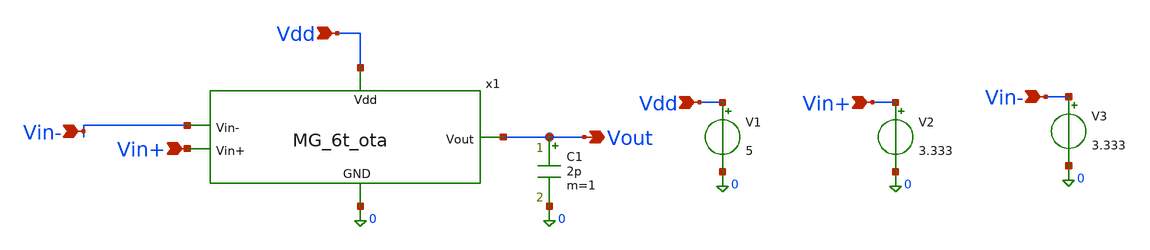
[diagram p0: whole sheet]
** sch_path: MG_6T_OTA/MG_6t_ota_testbench.sch
**.subckt MG_6t_ota_testbench Vdd Vin+ Vin- Vdd Vin+ Vin- Vout
*.ipin Vdd
*.ipin Vin+
*.ipin Vin-
*.ipin Vdd
*.ipin Vin+
*.ipin Vin-
*.opin Vout
V1 Vdd 0 5
V2 Vin+ 0 3.333
V3 Vin- 0 3.333
C1 Vout 0 2p m=1
x1 Vdd Vout Vin- Vin+ 0 MG_6t_ota
**** begin user architecture code



*.include /foss/pdks/gf180mcuD/libs.tech/ngspice/design.ngspice
*.lib /foss/pdks/gf180mcuD/libs.tech/ngspice/sm141064.ngspice typical
*.lib /foss/pdks/gf180mcuD/libs.tech/ngspice/sm141064.ngspice res_typical
*.lib /foss/pdks/gf180mcuD/libs.tech/ngspice/sm141064.ngspice moscap_typical
*.lib /foss/pdks/gf180mcuD/libs.tech/ngspice/sm141064.ngspice diode_typical

*.control
*  save all
*  op
*  alter v2 ac = 1
*  ac dec 20 1 1G
*  setplot ac1
*
*  let gain_db = vdb(vout)
*  let phase_deg = (180/PI) * ph(vout)
*
*  meas ac dc_gain MAX gain_db
*  meas ac ugbw WHEN gain_db=0 FALL=1
*  meas ac ph_at_ugbw FIND phase_deg WHEN gain_db=0
*  let phase_margin = 180 + ph_at_ugbw
*
*  print dc_gain ugbw phase_margin
*
*  plot gain_db title 'Magnitude Response (dB)'
*  plot phase_deg title 'Phase Response (Degrees)'
*.endc

.include /foss/pdks/gf180mcuD/libs.tech/ngspice/design.ngspice

* MUST be defined here exactly as 1
.param sw_stat_global=1
.param sw_stat_mismatch=1

.lib /foss/pdks/gf180mcuD/libs.tech/ngspice/sm141064.ngspice statistical
.lib /foss/pdks/gf180mcuD/libs.tech/ngspice/sm141064.ngspice res_statistical
.lib /foss/pdks/gf180mcuD/libs.tech/ngspice/sm141064.ngspice moscap_typical
.lib /foss/pdks/gf180mcuD/libs.tech/ngspice/sm141064.ngspice diode_typical

.control
  let mc_runs = 50
  let run_idx = 1

  echo Run_Number DC_Gain_dB UGBW_Hz Phase_Margin_Deg > mc_results.txt

  while run_idx <= mc_runs

    * 1. FLUSH THE CACHE: Turn off MC and reset
    * This forces NGSPICE to recognize a physical state change
    alterparam sw_stat_global = 0
    alterparam sw_stat_mismatch = 0
    reset

    * 2. ROLL NEW DICE: Change seed, turn MC back on exactly to 1, and reset
    * Because the state changed from 0 -> 1, NGSPICE is forced to re-evaluate
    * the agauss() functions with the new seed!
    setseed $&run_idx
    alterparam sw_stat_global = 1
    alterparam sw_stat_mismatch = 1
    reset

    op
    print all


    * 3. Run Simulation
    alter v2 ac = 1
    ac dec 20 1 1G


    * 4. Measure
    let gain_db = vdb(Vout)
    let phase_deg = (180/PI) * ph(Vout)

    meas ac dc_gain MAX gain_db
    meas ac ugbw WHEN gain_db=0 FALL=1
    meas ac ph_at_ugbw FIND phase_deg WHEN gain_db=0
    let phase_margin = 180 + ph_at_ugbw

    * 5. Save data
    echo $&run_idx $&dc_gain $&ugbw $&phase_margin >>
+ /foss/designs/C05-MRTMOS-SSCS-Chipathon/MG_6T_OTA/plots_and_results/mc_results.txt

    destroy all
    let run_idx = run_idx + 1
  end

  echo Monte Carlo simulation complete check mc_results.txt
.endc



**** end user architecture code
**.ends
.end
